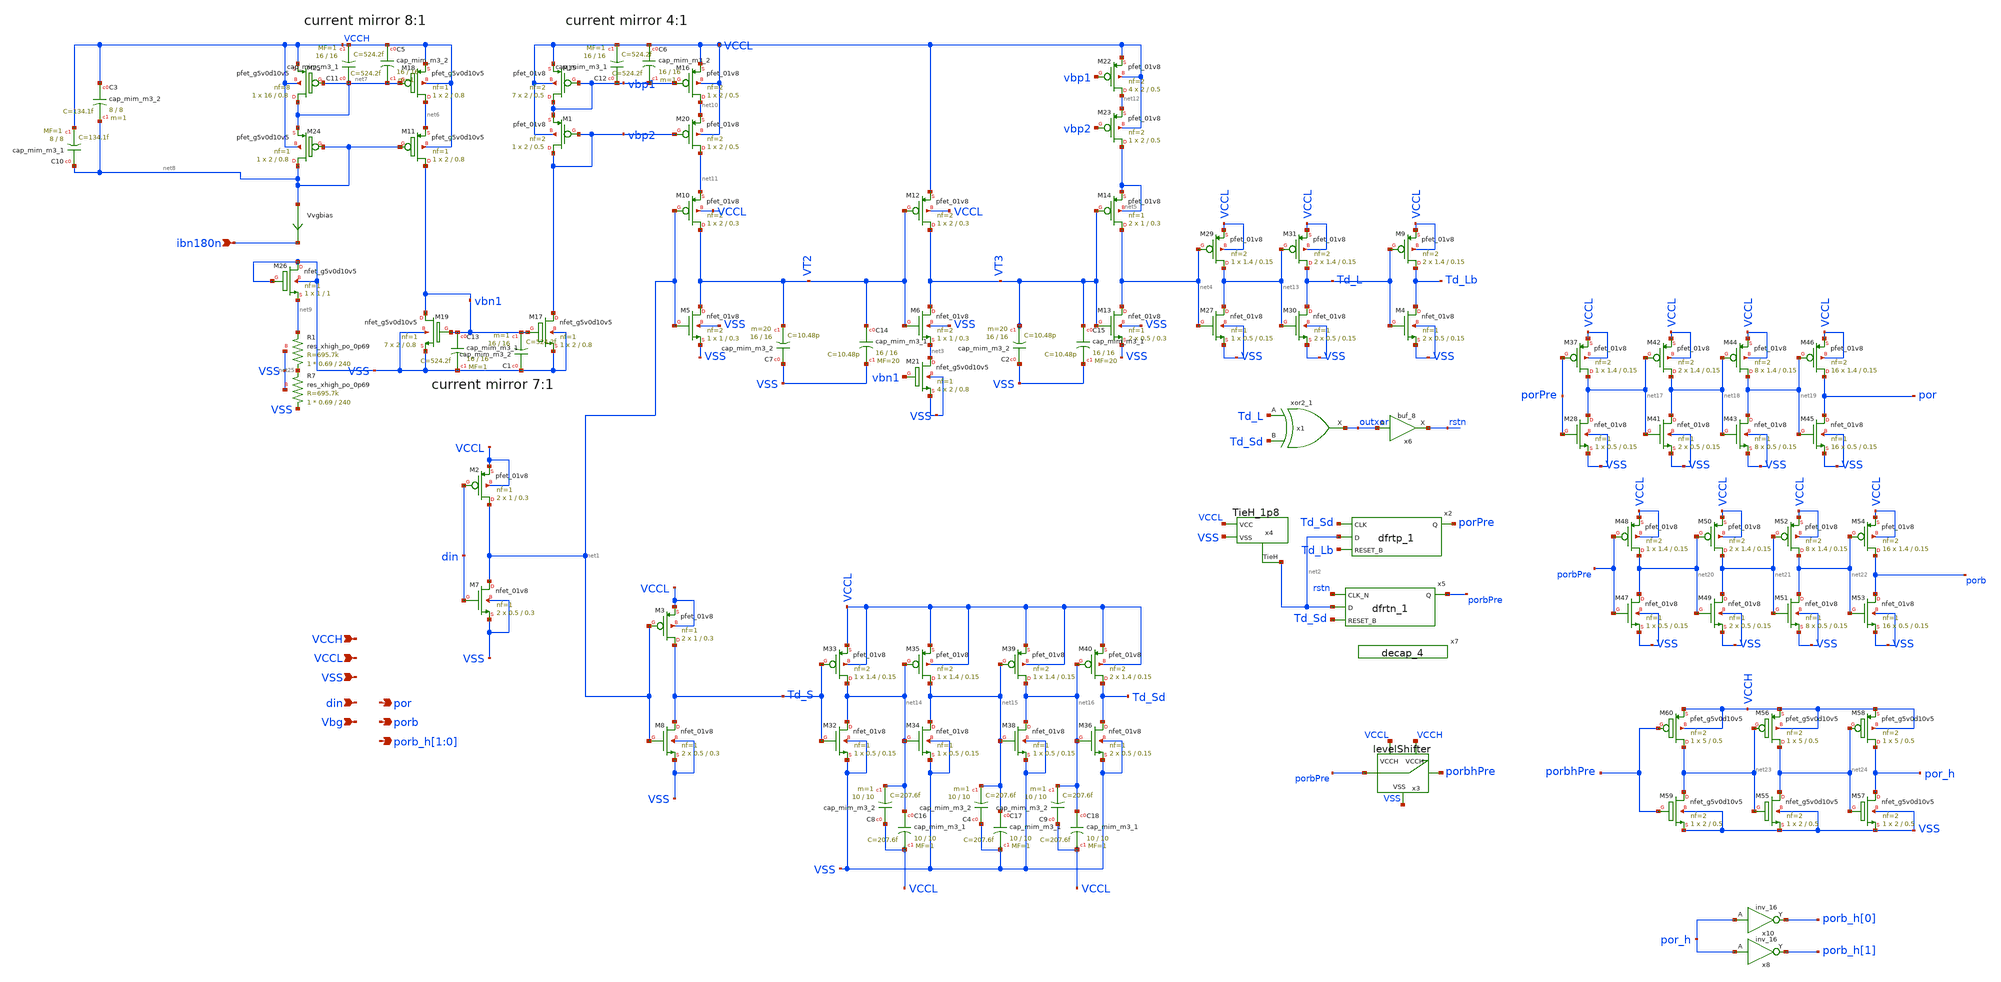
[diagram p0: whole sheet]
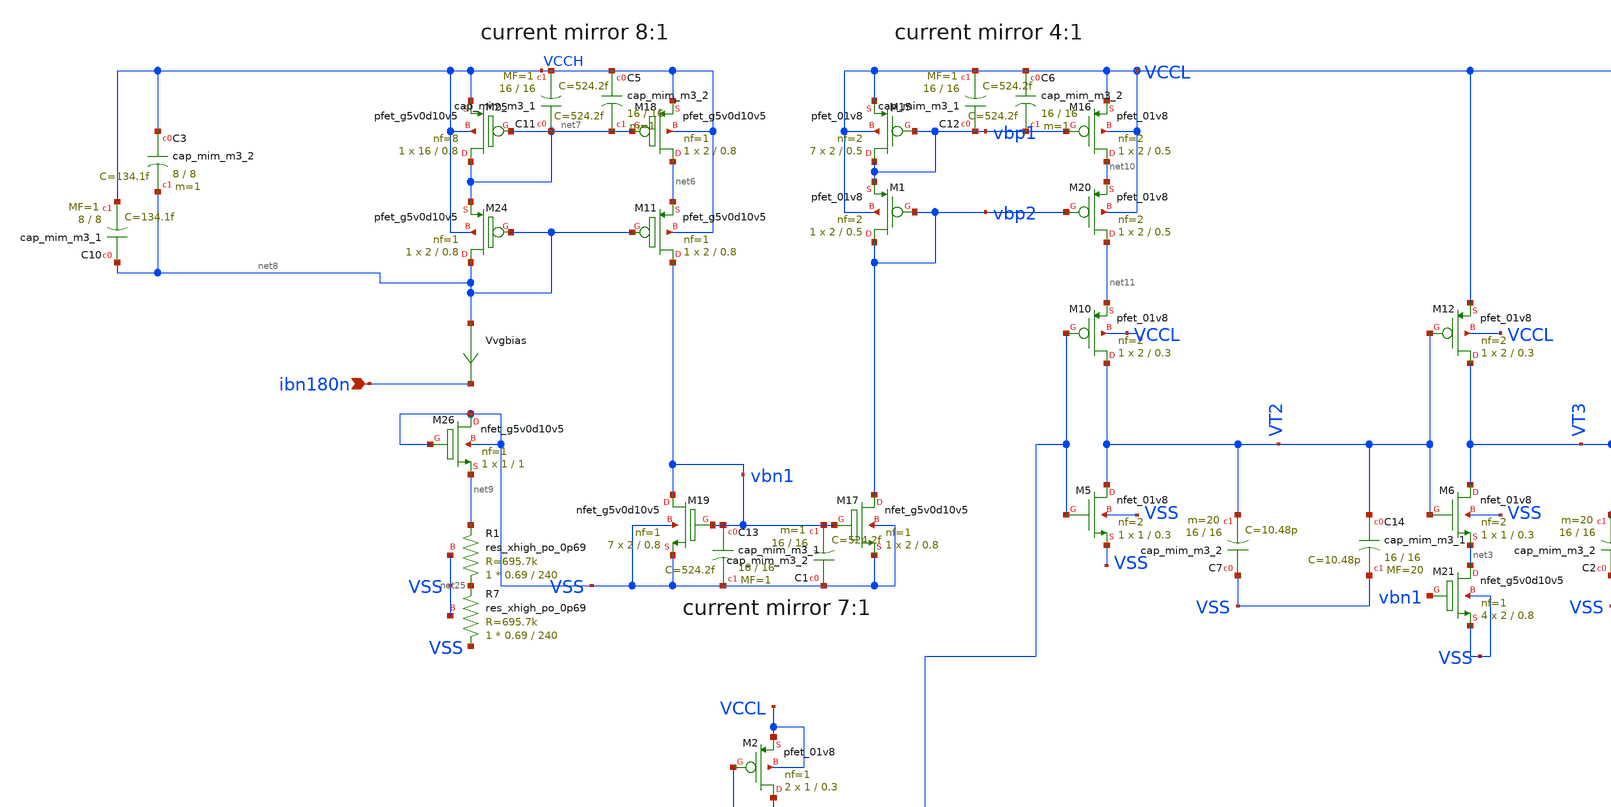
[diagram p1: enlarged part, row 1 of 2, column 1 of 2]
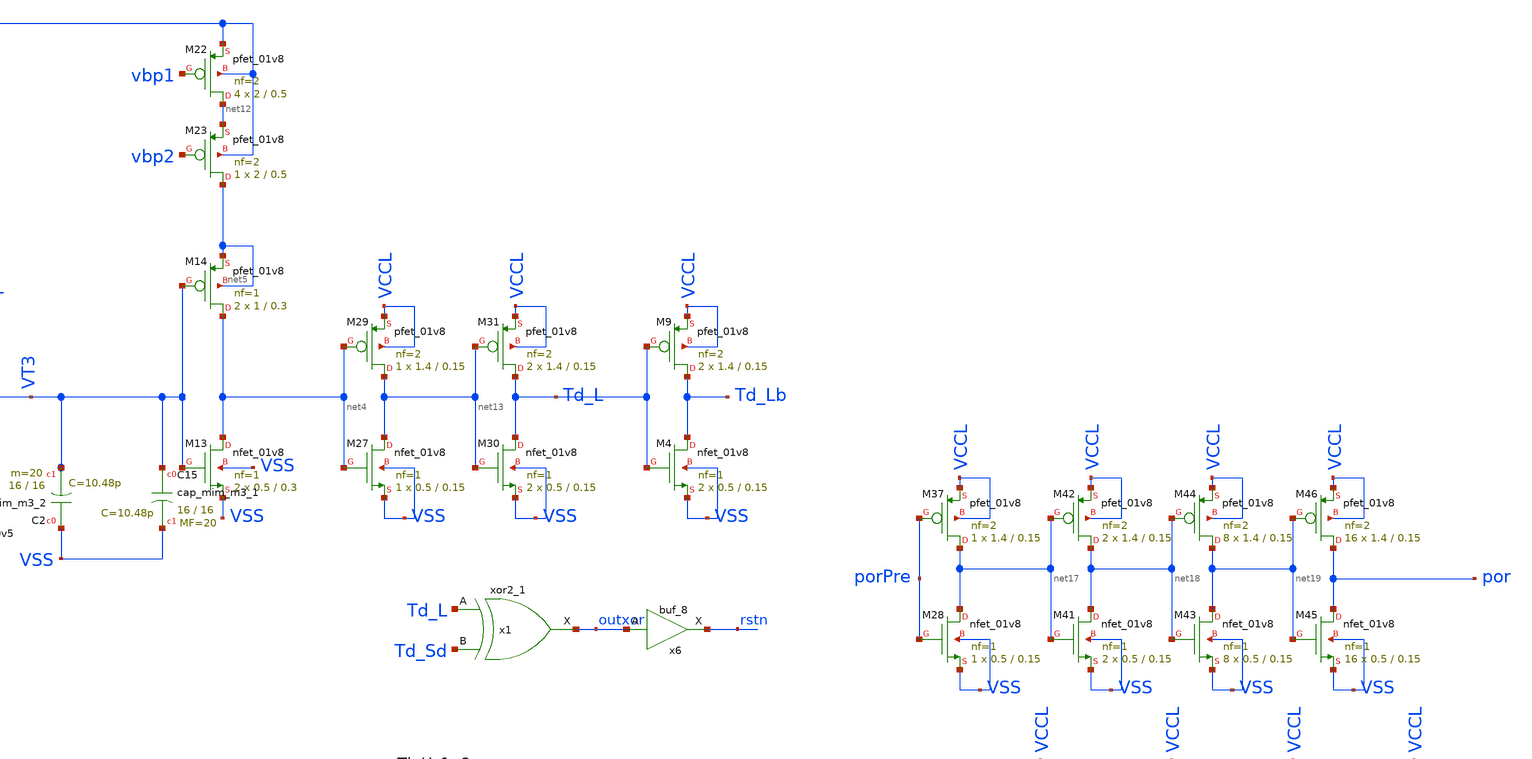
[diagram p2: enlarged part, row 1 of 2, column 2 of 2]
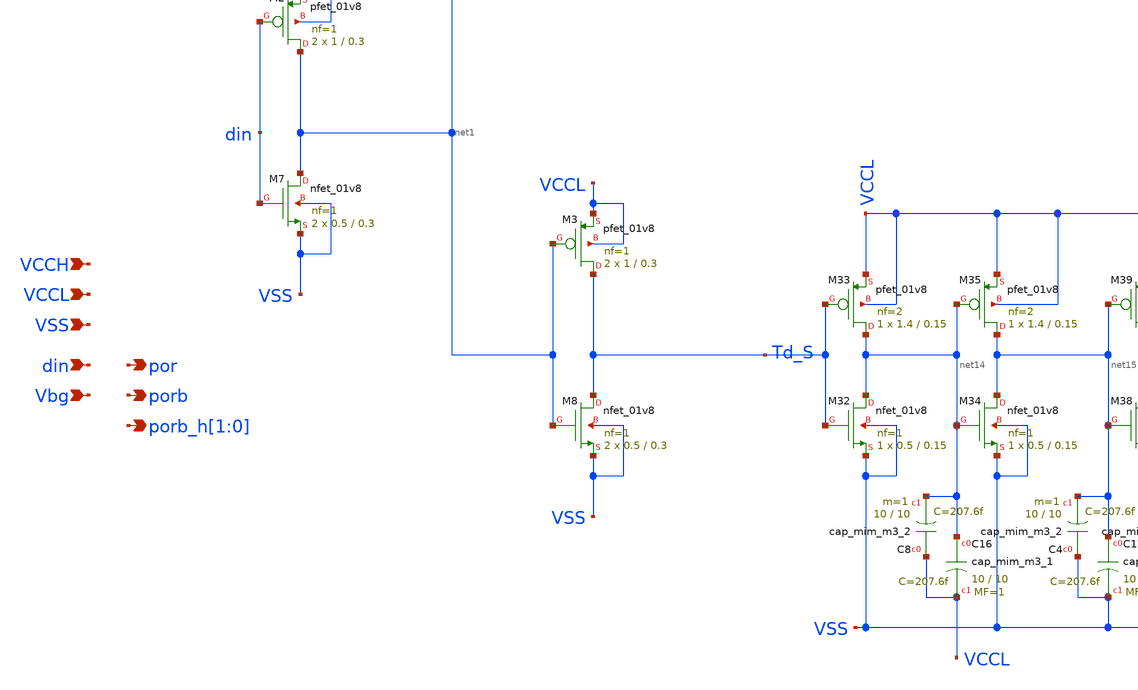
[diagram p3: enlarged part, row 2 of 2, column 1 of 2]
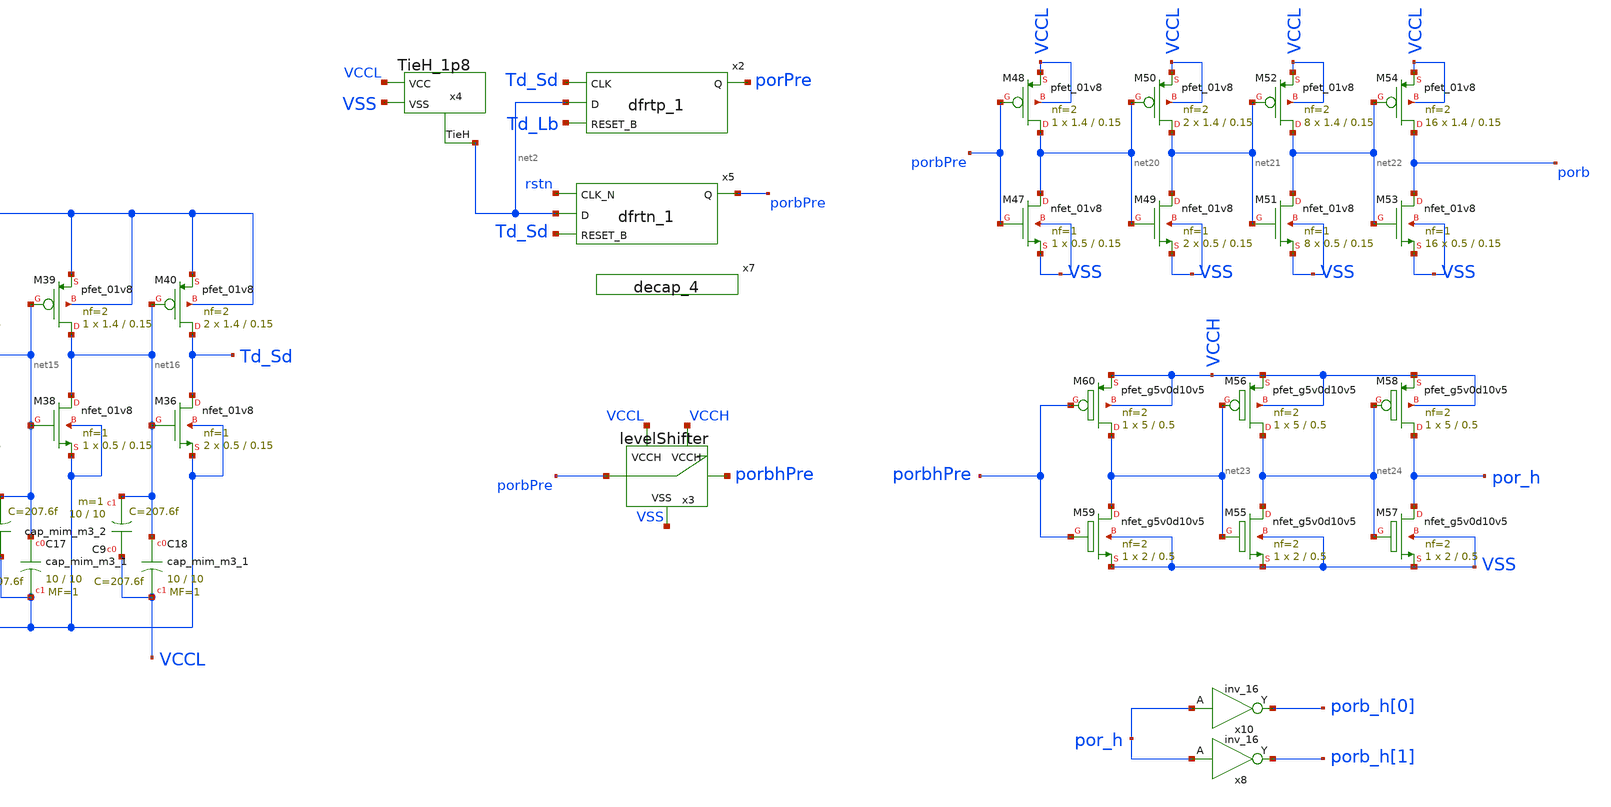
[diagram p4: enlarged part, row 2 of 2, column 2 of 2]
** sch_path: xschem/delayPulse_final.sch
**.subckt delayPulse_final VCCL VSS din Vbg por VCCH porb porb_h[1],porb_h[0] ibn180n
*.ipin VCCL
*.ipin VSS
*.ipin din
*.ipin Vbg
*.opin por
*.ipin VCCH
*.opin porb
*.opin porb_h[1],porb_h[0]
*.ipin ibn180n
x1 Td_L Td_Sd VSS VSS VCCL VCCL outxor sky130_fd_sc_ls__xor2_1
x3 porbPre porbhPre VCCL VSS VCCH levelShifter
XM2 net1 din VCCL VCCL sky130_fd_pr__pfet_01v8 L=0.3 W=1 nf=1 ad='int((nf+1)/2) * W/nf * 0.29' as='int((nf+2)/2) * W/nf * 0.29'
+ pd='2*int((nf+1)/2) * (W/nf + 0.29)' ps='2*int((nf+2)/2) * (W/nf + 0.29)' nrd='0.29 / W' nrs='0.29 / W'
+ sa=0 sb=0 sd=0 mult=2 m=2
XM3 Td_S net1 VCCL VCCL sky130_fd_pr__pfet_01v8 L=0.3 W=1 nf=1 ad='int((nf+1)/2) * W/nf * 0.29' as='int((nf+2)/2) * W/nf * 0.29'
+ pd='2*int((nf+1)/2) * (W/nf + 0.29)' ps='2*int((nf+2)/2) * (W/nf + 0.29)' nrd='0.29 / W' nrs='0.29 / W'
+ sa=0 sb=0 sd=0 mult=2 m=2
XM5 VT2 net1 VSS VSS sky130_fd_pr__nfet_01v8 L=0.3 W=1 nf=2 ad='int((nf+1)/2) * W/nf * 0.29' as='int((nf+2)/2) * W/nf * 0.29'
+ pd='2*int((nf+1)/2) * (W/nf + 0.29)' ps='2*int((nf+2)/2) * (W/nf + 0.29)' nrd='0.29 / W' nrs='0.29 / W'
+ sa=0 sb=0 sd=0 mult=1 m=1
XM7 net1 din VSS VSS sky130_fd_pr__nfet_01v8 L=0.3 W=0.5 nf=1 ad='int((nf+1)/2) * W/nf * 0.29' as='int((nf+2)/2) * W/nf * 0.29'
+ pd='2*int((nf+1)/2) * (W/nf + 0.29)' ps='2*int((nf+2)/2) * (W/nf + 0.29)' nrd='0.29 / W' nrs='0.29 / W'
+ sa=0 sb=0 sd=0 mult=2 m=2
XM8 Td_S net1 VSS VSS sky130_fd_pr__nfet_01v8 L=0.3 W=0.5 nf=1 ad='int((nf+1)/2) * W/nf * 0.29' as='int((nf+2)/2) * W/nf * 0.29'
+ pd='2*int((nf+1)/2) * (W/nf + 0.29)' ps='2*int((nf+2)/2) * (W/nf + 0.29)' nrd='0.29 / W' nrs='0.29 / W'
+ sa=0 sb=0 sd=0 mult=2 m=2
XM10 VT2 net1 net11 VCCL sky130_fd_pr__pfet_01v8 L=0.3 W=2 nf=2 ad='int((nf+1)/2) * W/nf * 0.29' as='int((nf+2)/2) * W/nf * 0.29'
+ pd='2*int((nf+1)/2) * (W/nf + 0.29)' ps='2*int((nf+2)/2) * (W/nf + 0.29)' nrd='0.29 / W' nrs='0.29 / W'
+ sa=0 sb=0 sd=0 mult=1 m=1
XM13 net4 VT3 VSS VSS sky130_fd_pr__nfet_01v8 L=0.3 W=0.5 nf=1 ad='int((nf+1)/2) * W/nf * 0.29' as='int((nf+2)/2) * W/nf * 0.29'
+ pd='2*int((nf+1)/2) * (W/nf + 0.29)' ps='2*int((nf+2)/2) * (W/nf + 0.29)' nrd='0.29 / W' nrs='0.29 / W'
+ sa=0 sb=0 sd=0 mult=2 m=2
XM14 net4 VT3 net5 net5 sky130_fd_pr__pfet_01v8 L=0.3 W=1 nf=1 ad='int((nf+1)/2) * W/nf * 0.29' as='int((nf+2)/2) * W/nf * 0.29'
+ pd='2*int((nf+1)/2) * (W/nf + 0.29)' ps='2*int((nf+2)/2) * (W/nf + 0.29)' nrd='0.29 / W' nrs='0.29 / W'
+ sa=0 sb=0 sd=0 mult=2 m=2
x4 net2 VSS VCCL TieH_1p8
XM11 vbn1 net8 net6 VCCH sky130_fd_pr__pfet_g5v0d10v5 L=0.8 W=2 nf=1 ad='int((nf+1)/2) * W/nf * 0.29'
+ as='int((nf+2)/2) * W/nf * 0.29' pd='2*int((nf+1)/2) * (W/nf + 0.29)' ps='2*int((nf+2)/2) * (W/nf + 0.29)'
+ nrd='0.29 / W' nrs='0.29 / W' sa=0 sb=0 sd=0 mult=1 m=1
XM17 vbp2 vbn1 VSS VSS sky130_fd_pr__nfet_g5v0d10v5 L=0.8 W=2 nf=1 ad='int((nf+1)/2) * W/nf * 0.29' as='int((nf+2)/2) * W/nf * 0.29'
+ pd='2*int((nf+1)/2) * (W/nf + 0.29)' ps='2*int((nf+2)/2) * (W/nf + 0.29)' nrd='0.29 / W' nrs='0.29 / W'
+ sa=0 sb=0 sd=0 mult=1 m=1
XM18 net6 net7 VCCH VCCH sky130_fd_pr__pfet_g5v0d10v5 L=0.8 W=2 nf=1 ad='int((nf+1)/2) * W/nf * 0.29'
+ as='int((nf+2)/2) * W/nf * 0.29' pd='2*int((nf+1)/2) * (W/nf + 0.29)' ps='2*int((nf+2)/2) * (W/nf + 0.29)'
+ nrd='0.29 / W' nrs='0.29 / W' sa=0 sb=0 sd=0 mult=1 m=1
XM19 vbn1 vbn1 VSS VSS sky130_fd_pr__nfet_g5v0d10v5 L=0.8 W=2 nf=1 ad='int((nf+1)/2) * W/nf * 0.29' as='int((nf+2)/2) * W/nf * 0.29'
+ pd='2*int((nf+1)/2) * (W/nf + 0.29)' ps='2*int((nf+2)/2) * (W/nf + 0.29)' nrd='0.29 / W' nrs='0.29 / W'
+ sa=0 sb=0 sd=0 mult=7 m=7
XM24 net8 net8 net7 VCCH sky130_fd_pr__pfet_g5v0d10v5 L=0.8 W=2 nf=1 ad='int((nf+1)/2) * W/nf * 0.29'
+ as='int((nf+2)/2) * W/nf * 0.29' pd='2*int((nf+1)/2) * (W/nf + 0.29)' ps='2*int((nf+2)/2) * (W/nf + 0.29)'
+ nrd='0.29 / W' nrs='0.29 / W' sa=0 sb=0 sd=0 mult=1 m=1
XM25 net7 net7 VCCH VCCH sky130_fd_pr__pfet_g5v0d10v5 L=0.8 W=16 nf=8 ad='int((nf+1)/2) * W/nf * 0.29'
+ as='int((nf+2)/2) * W/nf * 0.29' pd='2*int((nf+1)/2) * (W/nf + 0.29)' ps='2*int((nf+2)/2) * (W/nf + 0.29)'
+ nrd='0.29 / W' nrs='0.29 / W' sa=0 sb=0 sd=0 mult=1 m=1
XM26 VSS VSS net9 VSS sky130_fd_pr__nfet_g5v0d10v5 L=1 W=1 nf=1 ad='int((nf+1)/2) * W/nf * 0.29' as='int((nf+2)/2) * W/nf * 0.29'
+ pd='2*int((nf+1)/2) * (W/nf + 0.29)' ps='2*int((nf+2)/2) * (W/nf + 0.29)' nrd='0.29 / W' nrs='0.29 / W'
+ sa=0 sb=0 sd=0 mult=1 m=1
XM6 VT3 VT2 net3 VSS sky130_fd_pr__nfet_01v8 L=0.3 W=1 nf=2 ad='int((nf+1)/2) * W/nf * 0.29' as='int((nf+2)/2) * W/nf * 0.29'
+ pd='2*int((nf+1)/2) * (W/nf + 0.29)' ps='2*int((nf+2)/2) * (W/nf + 0.29)' nrd='0.29 / W' nrs='0.29 / W'
+ sa=0 sb=0 sd=0 mult=1 m=1
XM12 VT3 VT2 VCCL VCCL sky130_fd_pr__pfet_01v8 L=0.3 W=2 nf=2 ad='int((nf+1)/2) * W/nf * 0.29' as='int((nf+2)/2) * W/nf * 0.29'
+ pd='2*int((nf+1)/2) * (W/nf + 0.29)' ps='2*int((nf+2)/2) * (W/nf + 0.29)' nrd='0.29 / W' nrs='0.29 / W'
+ sa=0 sb=0 sd=0 mult=1 m=1
XM1 vbp2 vbp2 vbp1 VCCL sky130_fd_pr__pfet_01v8 L=0.5 W=2 nf=2 ad='int((nf+1)/2) * W/nf * 0.29' as='int((nf+2)/2) * W/nf * 0.29'
+ pd='2*int((nf+1)/2) * (W/nf + 0.29)' ps='2*int((nf+2)/2) * (W/nf + 0.29)' nrd='0.29 / W' nrs='0.29 / W'
+ sa=0 sb=0 sd=0 mult=1 m=1
XM15 vbp1 vbp1 VCCL VCCL sky130_fd_pr__pfet_01v8 L=0.5 W=2 nf=2 ad='int((nf+1)/2) * W/nf * 0.29' as='int((nf+2)/2) * W/nf * 0.29'
+ pd='2*int((nf+1)/2) * (W/nf + 0.29)' ps='2*int((nf+2)/2) * (W/nf + 0.29)' nrd='0.29 / W' nrs='0.29 / W'
+ sa=0 sb=0 sd=0 mult=7 m=7
XM16 net10 vbp1 VCCL VCCL sky130_fd_pr__pfet_01v8 L=0.5 W=2 nf=2 ad='int((nf+1)/2) * W/nf * 0.29' as='int((nf+2)/2) * W/nf * 0.29'
+ pd='2*int((nf+1)/2) * (W/nf + 0.29)' ps='2*int((nf+2)/2) * (W/nf + 0.29)' nrd='0.29 / W' nrs='0.29 / W'
+ sa=0 sb=0 sd=0 mult=1 m=1
XM20 net11 vbp2 net10 VCCL sky130_fd_pr__pfet_01v8 L=0.5 W=2 nf=2 ad='int((nf+1)/2) * W/nf * 0.29' as='int((nf+2)/2) * W/nf * 0.29'
+ pd='2*int((nf+1)/2) * (W/nf + 0.29)' ps='2*int((nf+2)/2) * (W/nf + 0.29)' nrd='0.29 / W' nrs='0.29 / W'
+ sa=0 sb=0 sd=0 mult=1 m=1
XM21 net3 vbn1 VSS VSS sky130_fd_pr__nfet_g5v0d10v5 L=0.8 W=2 nf=1 ad='int((nf+1)/2) * W/nf * 0.29' as='int((nf+2)/2) * W/nf * 0.29'
+ pd='2*int((nf+1)/2) * (W/nf + 0.29)' ps='2*int((nf+2)/2) * (W/nf + 0.29)' nrd='0.29 / W' nrs='0.29 / W'
+ sa=0 sb=0 sd=0 mult=4 m=4
XM22 net12 vbp1 VCCL VCCL sky130_fd_pr__pfet_01v8 L=0.5 W=2 nf=2 ad='int((nf+1)/2) * W/nf * 0.29' as='int((nf+2)/2) * W/nf * 0.29'
+ pd='2*int((nf+1)/2) * (W/nf + 0.29)' ps='2*int((nf+2)/2) * (W/nf + 0.29)' nrd='0.29 / W' nrs='0.29 / W'
+ sa=0 sb=0 sd=0 mult=4 m=4
XM23 net5 vbp2 net12 VCCL sky130_fd_pr__pfet_01v8 L=0.5 W=2 nf=2 ad='int((nf+1)/2) * W/nf * 0.29' as='int((nf+2)/2) * W/nf * 0.29'
+ pd='2*int((nf+1)/2) * (W/nf + 0.29)' ps='2*int((nf+2)/2) * (W/nf + 0.29)' nrd='0.29 / W' nrs='0.29 / W'
+ sa=0 sb=0 sd=0 mult=1 m=1
XM27 net13 net4 VSS VSS sky130_fd_pr__nfet_01v8 L=0.15 W=0.5 nf=1 ad='int((nf+1)/2) * W/nf * 0.29' as='int((nf+2)/2) * W/nf * 0.29'
+ pd='2*int((nf+1)/2) * (W/nf + 0.29)' ps='2*int((nf+2)/2) * (W/nf + 0.29)' nrd='0.29 / W' nrs='0.29 / W'
+ sa=0 sb=0 sd=0 mult=1 m=1
XM29 net13 net4 VCCL VCCL sky130_fd_pr__pfet_01v8 L=0.15 W=1.4 nf=2 ad='int((nf+1)/2) * W/nf * 0.29'
+ as='int((nf+2)/2) * W/nf * 0.29' pd='2*int((nf+1)/2) * (W/nf + 0.29)' ps='2*int((nf+2)/2) * (W/nf + 0.29)'
+ nrd='0.29 / W' nrs='0.29 / W' sa=0 sb=0 sd=0 mult=1 m=1
XM30 Td_L net13 VSS VSS sky130_fd_pr__nfet_01v8 L=0.15 W=0.5 nf=1 ad='int((nf+1)/2) * W/nf * 0.29' as='int((nf+2)/2) * W/nf * 0.29'
+ pd='2*int((nf+1)/2) * (W/nf + 0.29)' ps='2*int((nf+2)/2) * (W/nf + 0.29)' nrd='0.29 / W' nrs='0.29 / W'
+ sa=0 sb=0 sd=0 mult=2 m=2
XM31 Td_L net13 VCCL VCCL sky130_fd_pr__pfet_01v8 L=0.15 W=1.4 nf=2 ad='int((nf+1)/2) * W/nf * 0.29'
+ as='int((nf+2)/2) * W/nf * 0.29' pd='2*int((nf+1)/2) * (W/nf + 0.29)' ps='2*int((nf+2)/2) * (W/nf + 0.29)'
+ nrd='0.29 / W' nrs='0.29 / W' sa=0 sb=0 sd=0 mult=2 m=2
XM32 net14 Td_S VSS VSS sky130_fd_pr__nfet_01v8 L=0.15 W=0.5 nf=1 ad='int((nf+1)/2) * W/nf * 0.29' as='int((nf+2)/2) * W/nf * 0.29'
+ pd='2*int((nf+1)/2) * (W/nf + 0.29)' ps='2*int((nf+2)/2) * (W/nf + 0.29)' nrd='0.29 / W' nrs='0.29 / W'
+ sa=0 sb=0 sd=0 mult=1 m=1
XM33 net14 Td_S VCCL VCCL sky130_fd_pr__pfet_01v8 L=0.15 W=1.4 nf=2 ad='int((nf+1)/2) * W/nf * 0.29'
+ as='int((nf+2)/2) * W/nf * 0.29' pd='2*int((nf+1)/2) * (W/nf + 0.29)' ps='2*int((nf+2)/2) * (W/nf + 0.29)'
+ nrd='0.29 / W' nrs='0.29 / W' sa=0 sb=0 sd=0 mult=1 m=1
XM34 net15 net14 VSS VSS sky130_fd_pr__nfet_01v8 L=0.15 W=0.5 nf=1 ad='int((nf+1)/2) * W/nf * 0.29' as='int((nf+2)/2) * W/nf * 0.29'
+ pd='2*int((nf+1)/2) * (W/nf + 0.29)' ps='2*int((nf+2)/2) * (W/nf + 0.29)' nrd='0.29 / W' nrs='0.29 / W'
+ sa=0 sb=0 sd=0 mult=1 m=1
XM35 net15 net14 VCCL VCCL sky130_fd_pr__pfet_01v8 L=0.15 W=1.4 nf=2 ad='int((nf+1)/2) * W/nf * 0.29'
+ as='int((nf+2)/2) * W/nf * 0.29' pd='2*int((nf+1)/2) * (W/nf + 0.29)' ps='2*int((nf+2)/2) * (W/nf + 0.29)'
+ nrd='0.29 / W' nrs='0.29 / W' sa=0 sb=0 sd=0 mult=1 m=1
XM36 Td_Sd net16 VSS VSS sky130_fd_pr__nfet_01v8 L=0.15 W=0.5 nf=1 ad='int((nf+1)/2) * W/nf * 0.29' as='int((nf+2)/2) * W/nf * 0.29'
+ pd='2*int((nf+1)/2) * (W/nf + 0.29)' ps='2*int((nf+2)/2) * (W/nf + 0.29)' nrd='0.29 / W' nrs='0.29 / W'
+ sa=0 sb=0 sd=0 mult=2 m=2
XM38 net16 net15 VSS VSS sky130_fd_pr__nfet_01v8 L=0.15 W=0.5 nf=1 ad='int((nf+1)/2) * W/nf * 0.29' as='int((nf+2)/2) * W/nf * 0.29'
+ pd='2*int((nf+1)/2) * (W/nf + 0.29)' ps='2*int((nf+2)/2) * (W/nf + 0.29)' nrd='0.29 / W' nrs='0.29 / W'
+ sa=0 sb=0 sd=0 mult=1 m=1
XM39 net16 net15 VCCL VCCL sky130_fd_pr__pfet_01v8 L=0.15 W=1.4 nf=2 ad='int((nf+1)/2) * W/nf * 0.29'
+ as='int((nf+2)/2) * W/nf * 0.29' pd='2*int((nf+1)/2) * (W/nf + 0.29)' ps='2*int((nf+2)/2) * (W/nf + 0.29)'
+ nrd='0.29 / W' nrs='0.29 / W' sa=0 sb=0 sd=0 mult=1 m=1
x6 outxor VSS VSS VCCL VCCL rstn sky130_fd_sc_ls__buf_8
XC4 VSS net15 sky130_fd_pr__cap_mim_m3_2 W=10 L=10 MF=1 m=1
XC7 VSS VT2 sky130_fd_pr__cap_mim_m3_2 W=16 L=16 MF=20 m=20
XC2 VSS VT3 sky130_fd_pr__cap_mim_m3_2 W=16 L=16 MF=20 m=20
XC8 VCCL net14 sky130_fd_pr__cap_mim_m3_2 W=10 L=10 MF=1 m=1
XC9 VCCL net16 sky130_fd_pr__cap_mim_m3_2 W=10 L=10 MF=1 m=1
XM40 Td_Sd net16 VCCL VCCL sky130_fd_pr__pfet_01v8 L=0.15 W=1.4 nf=2 ad='int((nf+1)/2) * W/nf * 0.29'
+ as='int((nf+2)/2) * W/nf * 0.29' pd='2*int((nf+1)/2) * (W/nf + 0.29)' ps='2*int((nf+2)/2) * (W/nf + 0.29)'
+ nrd='0.29 / W' nrs='0.29 / W' sa=0 sb=0 sd=0 mult=2 m=2
x5 rstn net2 Td_Sd VSS VSS VCCL VCCL porbPre sky130_fd_sc_ls__dfrtn_1
x2 Td_Sd net2 Td_Lb VSS VSS VCCL VCCL porPre sky130_fd_sc_ls__dfrtp_1
XM4 Td_Lb Td_L VSS VSS sky130_fd_pr__nfet_01v8 L=0.15 W=0.5 nf=1 ad='int((nf+1)/2) * W/nf * 0.29' as='int((nf+2)/2) * W/nf * 0.29'
+ pd='2*int((nf+1)/2) * (W/nf + 0.29)' ps='2*int((nf+2)/2) * (W/nf + 0.29)' nrd='0.29 / W' nrs='0.29 / W'
+ sa=0 sb=0 sd=0 mult=2 m=2
XM9 Td_Lb Td_L VCCL VCCL sky130_fd_pr__pfet_01v8 L=0.15 W=1.4 nf=2 ad='int((nf+1)/2) * W/nf * 0.29' as='int((nf+2)/2) * W/nf * 0.29'
+ pd='2*int((nf+1)/2) * (W/nf + 0.29)' ps='2*int((nf+2)/2) * (W/nf + 0.29)' nrd='0.29 / W' nrs='0.29 / W'
+ sa=0 sb=0 sd=0 mult=2 m=2
XC1 VSS vbn1 sky130_fd_pr__cap_mim_m3_2 W=16 L=16 MF=1 m=1
XC5 VCCH net7 sky130_fd_pr__cap_mim_m3_2 W=16 L=16 MF=1 m=1
XC6 VCCL vbp1 sky130_fd_pr__cap_mim_m3_2 W=16 L=16 MF=1 m=1
XC3 VCCH net8 sky130_fd_pr__cap_mim_m3_2 W=8 L=8 MF=1 m=1
XM28 net17 porPre VSS VSS sky130_fd_pr__nfet_01v8 L=0.15 W=0.5 nf=1 ad='int((nf+1)/2) * W/nf * 0.29'
+ as='int((nf+2)/2) * W/nf * 0.29' pd='2*int((nf+1)/2) * (W/nf + 0.29)' ps='2*int((nf+2)/2) * (W/nf + 0.29)'
+ nrd='0.29 / W' nrs='0.29 / W' sa=0 sb=0 sd=0 mult=1 m=1
XM37 net17 porPre VCCL VCCL sky130_fd_pr__pfet_01v8 L=0.15 W=1.4 nf=2 ad='int((nf+1)/2) * W/nf * 0.29'
+ as='int((nf+2)/2) * W/nf * 0.29' pd='2*int((nf+1)/2) * (W/nf + 0.29)' ps='2*int((nf+2)/2) * (W/nf + 0.29)'
+ nrd='0.29 / W' nrs='0.29 / W' sa=0 sb=0 sd=0 mult=1 m=1
XM41 net18 net17 VSS VSS sky130_fd_pr__nfet_01v8 L=0.15 W=0.5 nf=1 ad='int((nf+1)/2) * W/nf * 0.29' as='int((nf+2)/2) * W/nf * 0.29'
+ pd='2*int((nf+1)/2) * (W/nf + 0.29)' ps='2*int((nf+2)/2) * (W/nf + 0.29)' nrd='0.29 / W' nrs='0.29 / W'
+ sa=0 sb=0 sd=0 mult=2 m=2
XM42 net18 net17 VCCL VCCL sky130_fd_pr__pfet_01v8 L=0.15 W=1.4 nf=2 ad='int((nf+1)/2) * W/nf * 0.29'
+ as='int((nf+2)/2) * W/nf * 0.29' pd='2*int((nf+1)/2) * (W/nf + 0.29)' ps='2*int((nf+2)/2) * (W/nf + 0.29)'
+ nrd='0.29 / W' nrs='0.29 / W' sa=0 sb=0 sd=0 mult=2 m=2
XM43 net19 net18 VSS VSS sky130_fd_pr__nfet_01v8 L=0.15 W=0.5 nf=1 ad='int((nf+1)/2) * W/nf * 0.29' as='int((nf+2)/2) * W/nf * 0.29'
+ pd='2*int((nf+1)/2) * (W/nf + 0.29)' ps='2*int((nf+2)/2) * (W/nf + 0.29)' nrd='0.29 / W' nrs='0.29 / W'
+ sa=0 sb=0 sd=0 mult=8 m=8
XM44 net19 net18 VCCL VCCL sky130_fd_pr__pfet_01v8 L=0.15 W=1.4 nf=2 ad='int((nf+1)/2) * W/nf * 0.29'
+ as='int((nf+2)/2) * W/nf * 0.29' pd='2*int((nf+1)/2) * (W/nf + 0.29)' ps='2*int((nf+2)/2) * (W/nf + 0.29)'
+ nrd='0.29 / W' nrs='0.29 / W' sa=0 sb=0 sd=0 mult=8 m=8
XM45 por net19 VSS VSS sky130_fd_pr__nfet_01v8 L=0.15 W=0.5 nf=1 ad='int((nf+1)/2) * W/nf * 0.29' as='int((nf+2)/2) * W/nf * 0.29'
+ pd='2*int((nf+1)/2) * (W/nf + 0.29)' ps='2*int((nf+2)/2) * (W/nf + 0.29)' nrd='0.29 / W' nrs='0.29 / W'
+ sa=0 sb=0 sd=0 mult=16 m=16
XM46 por net19 VCCL VCCL sky130_fd_pr__pfet_01v8 L=0.15 W=1.4 nf=2 ad='int((nf+1)/2) * W/nf * 0.29' as='int((nf+2)/2) * W/nf * 0.29'
+ pd='2*int((nf+1)/2) * (W/nf + 0.29)' ps='2*int((nf+2)/2) * (W/nf + 0.29)' nrd='0.29 / W' nrs='0.29 / W'
+ sa=0 sb=0 sd=0 mult=16 m=16
XM47 net20 porbPre VSS VSS sky130_fd_pr__nfet_01v8 L=0.15 W=0.5 nf=1 ad='int((nf+1)/2) * W/nf * 0.29'
+ as='int((nf+2)/2) * W/nf * 0.29' pd='2*int((nf+1)/2) * (W/nf + 0.29)' ps='2*int((nf+2)/2) * (W/nf + 0.29)'
+ nrd='0.29 / W' nrs='0.29 / W' sa=0 sb=0 sd=0 mult=1 m=1
XM48 net20 porbPre VCCL VCCL sky130_fd_pr__pfet_01v8 L=0.15 W=1.4 nf=2 ad='int((nf+1)/2) * W/nf * 0.29'
+ as='int((nf+2)/2) * W/nf * 0.29' pd='2*int((nf+1)/2) * (W/nf + 0.29)' ps='2*int((nf+2)/2) * (W/nf + 0.29)'
+ nrd='0.29 / W' nrs='0.29 / W' sa=0 sb=0 sd=0 mult=1 m=1
XM49 net21 net20 VSS VSS sky130_fd_pr__nfet_01v8 L=0.15 W=0.5 nf=1 ad='int((nf+1)/2) * W/nf * 0.29' as='int((nf+2)/2) * W/nf * 0.29'
+ pd='2*int((nf+1)/2) * (W/nf + 0.29)' ps='2*int((nf+2)/2) * (W/nf + 0.29)' nrd='0.29 / W' nrs='0.29 / W'
+ sa=0 sb=0 sd=0 mult=2 m=2
XM50 net21 net20 VCCL VCCL sky130_fd_pr__pfet_01v8 L=0.15 W=1.4 nf=2 ad='int((nf+1)/2) * W/nf * 0.29'
+ as='int((nf+2)/2) * W/nf * 0.29' pd='2*int((nf+1)/2) * (W/nf + 0.29)' ps='2*int((nf+2)/2) * (W/nf + 0.29)'
+ nrd='0.29 / W' nrs='0.29 / W' sa=0 sb=0 sd=0 mult=2 m=2
XM51 net22 net21 VSS VSS sky130_fd_pr__nfet_01v8 L=0.15 W=0.5 nf=1 ad='int((nf+1)/2) * W/nf * 0.29' as='int((nf+2)/2) * W/nf * 0.29'
+ pd='2*int((nf+1)/2) * (W/nf + 0.29)' ps='2*int((nf+2)/2) * (W/nf + 0.29)' nrd='0.29 / W' nrs='0.29 / W'
+ sa=0 sb=0 sd=0 mult=8 m=8
XM52 net22 net21 VCCL VCCL sky130_fd_pr__pfet_01v8 L=0.15 W=1.4 nf=2 ad='int((nf+1)/2) * W/nf * 0.29'
+ as='int((nf+2)/2) * W/nf * 0.29' pd='2*int((nf+1)/2) * (W/nf + 0.29)' ps='2*int((nf+2)/2) * (W/nf + 0.29)'
+ nrd='0.29 / W' nrs='0.29 / W' sa=0 sb=0 sd=0 mult=8 m=8
XM53 porb net22 VSS VSS sky130_fd_pr__nfet_01v8 L=0.15 W=0.5 nf=1 ad='int((nf+1)/2) * W/nf * 0.29' as='int((nf+2)/2) * W/nf * 0.29'
+ pd='2*int((nf+1)/2) * (W/nf + 0.29)' ps='2*int((nf+2)/2) * (W/nf + 0.29)' nrd='0.29 / W' nrs='0.29 / W'
+ sa=0 sb=0 sd=0 mult=16 m=16
XM54 porb net22 VCCL VCCL sky130_fd_pr__pfet_01v8 L=0.15 W=1.4 nf=2 ad='int((nf+1)/2) * W/nf * 0.29'
+ as='int((nf+2)/2) * W/nf * 0.29' pd='2*int((nf+1)/2) * (W/nf + 0.29)' ps='2*int((nf+2)/2) * (W/nf + 0.29)'
+ nrd='0.29 / W' nrs='0.29 / W' sa=0 sb=0 sd=0 mult=16 m=16
XM59 net23 porbhPre VSS VSS sky130_fd_pr__nfet_g5v0d10v5 L=0.5 W=2 nf=2 ad='int((nf+1)/2) * W/nf * 0.29'
+ as='int((nf+2)/2) * W/nf * 0.29' pd='2*int((nf+1)/2) * (W/nf + 0.29)' ps='2*int((nf+2)/2) * (W/nf + 0.29)'
+ nrd='0.29 / W' nrs='0.29 / W' sa=0 sb=0 sd=0 mult=1 m=1
XM60 net23 porbhPre VCCH VCCH sky130_fd_pr__pfet_g5v0d10v5 L=0.5 W=5 nf=2 ad='int((nf+1)/2) * W/nf * 0.29'
+ as='int((nf+2)/2) * W/nf * 0.29' pd='2*int((nf+1)/2) * (W/nf + 0.29)' ps='2*int((nf+2)/2) * (W/nf + 0.29)'
+ nrd='0.29 / W' nrs='0.29 / W' sa=0 sb=0 sd=0 mult=1 m=1
x7 VSS VSS VCCL VCCL sky130_fd_sc_ls__decap_4
XC10 net8 VCCH sky130_fd_pr__cap_mim_m3_1 W=8 L=8 MF=1 m=1
XC11 net7 VCCH sky130_fd_pr__cap_mim_m3_1 W=16 L=16 MF=1 m=1
XC12 vbp1 VCCL sky130_fd_pr__cap_mim_m3_1 W=16 L=16 MF=1 m=1
XC13 vbn1 VSS sky130_fd_pr__cap_mim_m3_1 W=16 L=16 MF=1 m=1
XC14 VT2 VSS sky130_fd_pr__cap_mim_m3_1 W=16 L=16 MF=20 m=20
XC15 VT3 VSS sky130_fd_pr__cap_mim_m3_1 W=16 L=16 MF=20 m=20
XC16 net14 VCCL sky130_fd_pr__cap_mim_m3_1 W=10 L=10 MF=1 m=1
XC17 net15 VSS sky130_fd_pr__cap_mim_m3_1 W=10 L=10 MF=1 m=1
XC18 net16 VCCL sky130_fd_pr__cap_mim_m3_1 W=10 L=10 MF=1 m=1
XR1 net25 net9 VSS sky130_fd_pr__res_xhigh_po_0p69 L=240 mult=1 m=1
XR7 VSS net25 VSS sky130_fd_pr__res_xhigh_po_0p69 L=240 mult=1 m=1
XM55 net24 net23 VSS VSS sky130_fd_pr__nfet_g5v0d10v5 L=0.5 W=2 nf=2 ad='int((nf+1)/2) * W/nf * 0.29'
+ as='int((nf+2)/2) * W/nf * 0.29' pd='2*int((nf+1)/2) * (W/nf + 0.29)' ps='2*int((nf+2)/2) * (W/nf + 0.29)'
+ nrd='0.29 / W' nrs='0.29 / W' sa=0 sb=0 sd=0 mult=1 m=1
XM56 net24 net23 VCCH VCCH sky130_fd_pr__pfet_g5v0d10v5 L=0.5 W=5 nf=2 ad='int((nf+1)/2) * W/nf * 0.29'
+ as='int((nf+2)/2) * W/nf * 0.29' pd='2*int((nf+1)/2) * (W/nf + 0.29)' ps='2*int((nf+2)/2) * (W/nf + 0.29)'
+ nrd='0.29 / W' nrs='0.29 / W' sa=0 sb=0 sd=0 mult=1 m=1
XM57 por_h net24 VSS VSS sky130_fd_pr__nfet_g5v0d10v5 L=0.5 W=2 nf=2 ad='int((nf+1)/2) * W/nf * 0.29'
+ as='int((nf+2)/2) * W/nf * 0.29' pd='2*int((nf+1)/2) * (W/nf + 0.29)' ps='2*int((nf+2)/2) * (W/nf + 0.29)'
+ nrd='0.29 / W' nrs='0.29 / W' sa=0 sb=0 sd=0 mult=1 m=1
XM58 por_h net24 VCCH VCCH sky130_fd_pr__pfet_g5v0d10v5 L=0.5 W=5 nf=2 ad='int((nf+1)/2) * W/nf * 0.29'
+ as='int((nf+2)/2) * W/nf * 0.29' pd='2*int((nf+1)/2) * (W/nf + 0.29)' ps='2*int((nf+2)/2) * (W/nf + 0.29)'
+ nrd='0.29 / W' nrs='0.29 / W' sa=0 sb=0 sd=0 mult=1 m=1
x10 por_h VSS VSS VCCH VCCH porb_h[0] sky130_fd_sc_hvl__inv_16
x8 por_h VSS VSS VCCH VCCH porb_h[1] sky130_fd_sc_hvl__inv_16
Vvgbias net8 ibn180n 0
.save i(vvgbias)
**.ends
.end
